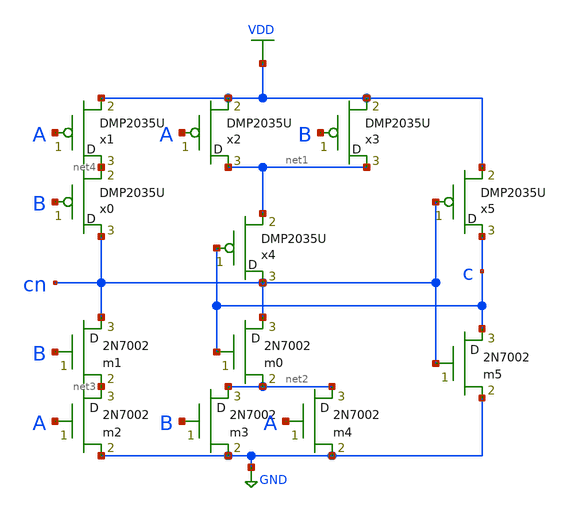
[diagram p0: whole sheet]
** sch_path: cells/xschem/ASYNC1.sch
**.subckt ASYNC1
m1 cn B net3 enbsim3 m=1
x1 net4 A VDD epbsim3 m=1
x0 cn B net4 epbsim3 m=1
x2 net1 A VDD epbsim3 m=1
x3 net1 B VDD epbsim3 m=1
x4 cn c net1 epbsim3 m=1
x5 c cn VDD epbsim3 m=1
m0 cn c net2 enbsim3 m=1
m2 net3 A GND enbsim3 m=1
m3 net2 B GND enbsim3 m=1
m4 net2 A GND enbsim3 m=1
m5 c cn GND enbsim3 m=1
**.ends
.GLOBAL GND
.GLOBAL VDD
.end
